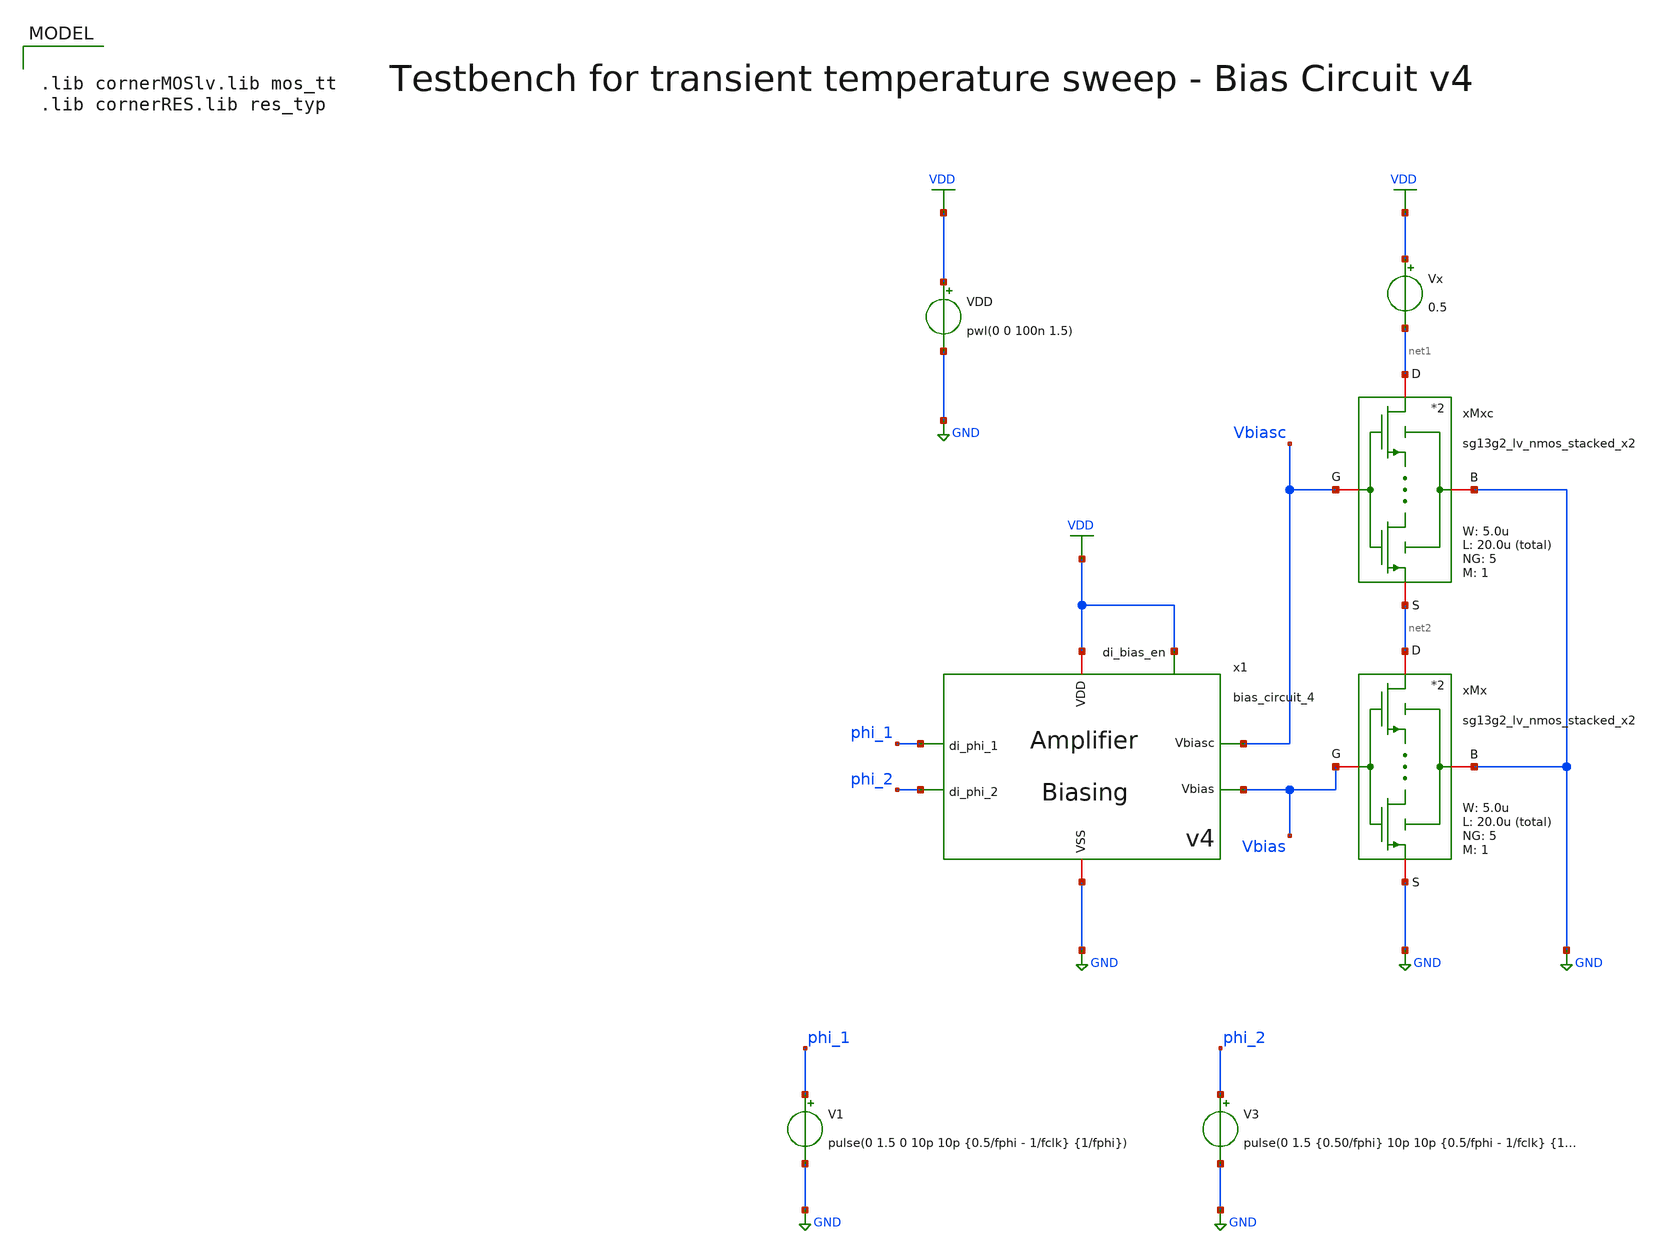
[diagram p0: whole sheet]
** sch_path: SG13G2_ATBS-ADC-main/xschem/bio_amplifier/amplifier_core/bias_circuit/bias_circuit_4/testbenches/bias_circuit_4_tb_temp_tran.sch
**.subckt bias_circuit_4_tb_temp_tran
x1 phi_2 phi_1 VDD GND Vbiasc Vbias VDD bias_circuit_4
V1 phi_1 GND pulse(0 1.5 0 10p 10p {0.5/fphi - 1/fclk} {1/fphi})
V3 phi_2 GND pulse(0 1.5 {0.50/fphi} 10p 10p {0.5/fphi - 1/fclk} {1/fphi})
Vx VDD net1 0.5
xMx net2 Vbias GND GND sg13g2_lv_nmos_stacked_x2 W_N=5.0u L_N=20.0u NG_N=5 M_N=1
xMxc net1 Vbiasc GND net2 sg13g2_lv_nmos_stacked_x2 W_N=5.0u L_N=20.0u NG_N=5 M_N=1
VDD VDD GND pwl(0 0 100n 1.5)
**** begin user architecture code

.lib cornerMOSlv.lib mos_tt
.lib cornerRES.lib res_typ



.param fclk=8000000
.param fphi=62500
.csparam fclk=fclk
.options klu method=gear reltol=1e-3 abstol=1e-15 gmin=1e-15
.control

* save all
save v(Vbias) v(Vbiasc) i(Vx) i(v.x1.viout) i(v.x1.viref)

setplot const

set wr_vecnames
set wr_singlescale

* User constants
let tstep = 1/fclk
let tstop = 500u

* Define temperature and Vref vectors
* Commercial Temperature Range
compose temp_vec start=0 stop=70 step=2
let vbias_vec=vector(length(temp_vec))
let vbiasc_vec=vector(length(temp_vec))
let iref_vec=vector(length(temp_vec))
let iout_vec=vector(length(temp_vec))
let ix_vec=vector(length(temp_vec))

* Loop index
let idx = 0

* For-Loop
foreach temp_val $&temp_vec
  * Adapt temperature
  option temp=$temp_val

  * Transient Analysis
  tran $&const.tstep $&const.tstop
  write bias_circuit_4_tb_temp_tran.raw
  set appendwrite

  * Measurement
  meas tran vbias FIND v(Vbias) AT=$&const.tstop
  meas tran vbiasc FIND v(Vbiasc) AT=$&const.tstop
  meas tran iref FIND i(v.x1.viref) AT=$&const.tstop
  meas tran iout FIND i(v.x1.viout) AT=$&const.tstop
  meas tran ix FIND i(Vx) AT=$&const.tstop

  * Append to vector
  let const.vbias_vec[const.idx] = vbias
  let const.vbiasc_vec[const.idx] = vbiasc
  let const.iref_vec[const.idx] = iref
  let const.iout_vec[const.idx] = iout
  let const.ix_vec[const.idx] = ix

  * Update index
  let const.idx = const.idx + 1
  echo ======================================================
end

print const.temp_vec
print const.vbias_vec
print const.vbiasc_vec
print const.iref_vec
print const.iout_vec
print const.ix_vec

* Setscale for plot against temperature
setscale const.vbias_vec const.temp_vec
setscale const.vbiasc_vec const.temp_vec
setscale const.iref_vec const.temp_vec
setscale const.iout_vec const.temp_vec
setscale const.ix_vec const.temp_vec

* Plot Vbias vs. temperature
plot const.vbias_vec title 'Vbias vs T' ylabel 'V'

* Plot Vbiasc vs. temperature
plot const.vbiasc_vec title 'Vbiasc vs T' ylabel 'V'

* Plot Iref vs. temperature
plot const.iref_vec title 'Iref vs T' ylabel 'A'

* Plot Iout vs. temperature
plot const.iout_vec title 'Iout vs T' ylabel 'A'

* Plot Ix vs. temperature
plot const.ix_vec title 'Ix vs T' ylabel 'A'

* Write Data
wrdata
+ /foss/designs/SG13G2_ATBS-ADC-main/python/plot_simulations/data/bias_circuit_4_tb_temp_tran.txt v(const.vbias_vec) v(const.vbiasc_vec) v(const.iref_vec) v(const.iout_vec) v(const.ix_vec)

*quit
.endc

**** end user architecture code
**.ends
.GLOBAL GND
.GLOBAL VDD
.end
